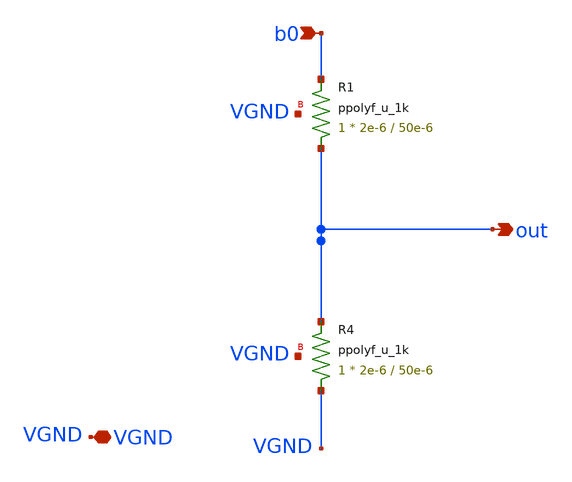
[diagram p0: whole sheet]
** sch_path: xschem/r2r_simple.sch
**.subckt r2r_simple VGND b0 out
*.iopin VGND
*.ipin b0
*.opin out
XR1 out b0 VGND ppolyf_u_1k r_width=2e-6 r_length=50e-6 m=1
XR4 VGND out VGND ppolyf_u_1k r_width=2e-6 r_length=50e-6 m=1
**.ends
.end
